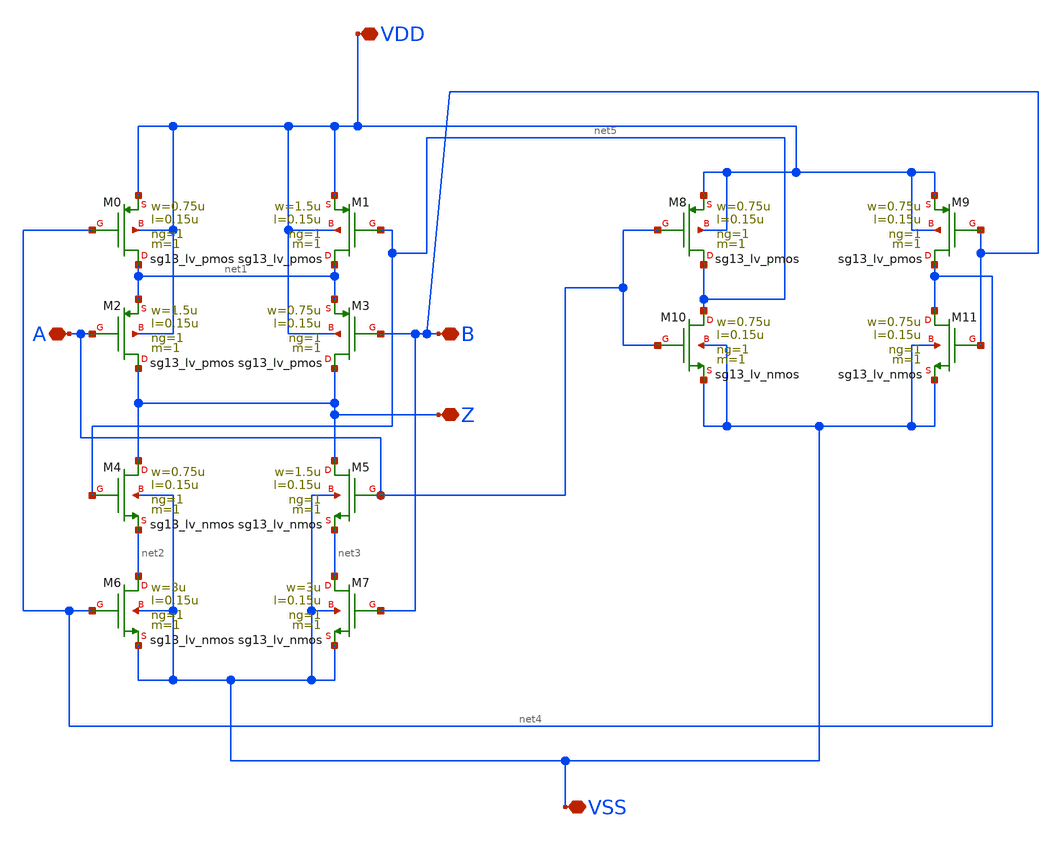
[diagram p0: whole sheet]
** sch_path: blocks/xor-g/xor-g.sch
**.subckt xor-g B A Z VSS VDD
*.iopin B
*.iopin A
*.iopin Z
*.iopin VSS
*.iopin VDD
XM0 net1 net4 VDD VDD sg13_lv_pmos w=0.75u l=0.15u ng=1 m=1 mm_ok=1
XM1 net1 net5 VDD VDD sg13_lv_pmos w=1.5u l=0.15u ng=1 m=1 mm_ok=1
XM2 Z A net1 VDD sg13_lv_pmos w=1.5u l=0.15u ng=1 m=1 mm_ok=1
XM3 Z B net1 VDD sg13_lv_pmos w=0.75u l=0.15u ng=1 m=1 mm_ok=1
XM4 Z net5 net2 VSS sg13_lv_nmos w=0.75u l=0.15u ng=1 m=1 mm_ok=1
XM5 Z A net3 VSS sg13_lv_nmos w=1.5u l=0.15u ng=1 m=1 mm_ok=1
XM6 net2 net4 VSS VSS sg13_lv_nmos w=3u l=0.15u ng=1 m=1 mm_ok=1
XM7 net3 B VSS VSS sg13_lv_nmos w=3u l=0.15u ng=1 m=1 mm_ok=1
XM8 net5 A VDD VDD sg13_lv_pmos w=0.75u l=0.15u ng=1 m=1 mm_ok=1
XM9 net4 B VDD VDD sg13_lv_pmos w=0.75u l=0.15u ng=1 m=1 mm_ok=1
XM10 net5 A VSS VSS sg13_lv_nmos w=0.75u l=0.15u ng=1 m=1 mm_ok=1
XM11 net4 B VSS VSS sg13_lv_nmos w=0.75u l=0.15u ng=1 m=1 mm_ok=1
**.ends
.end
